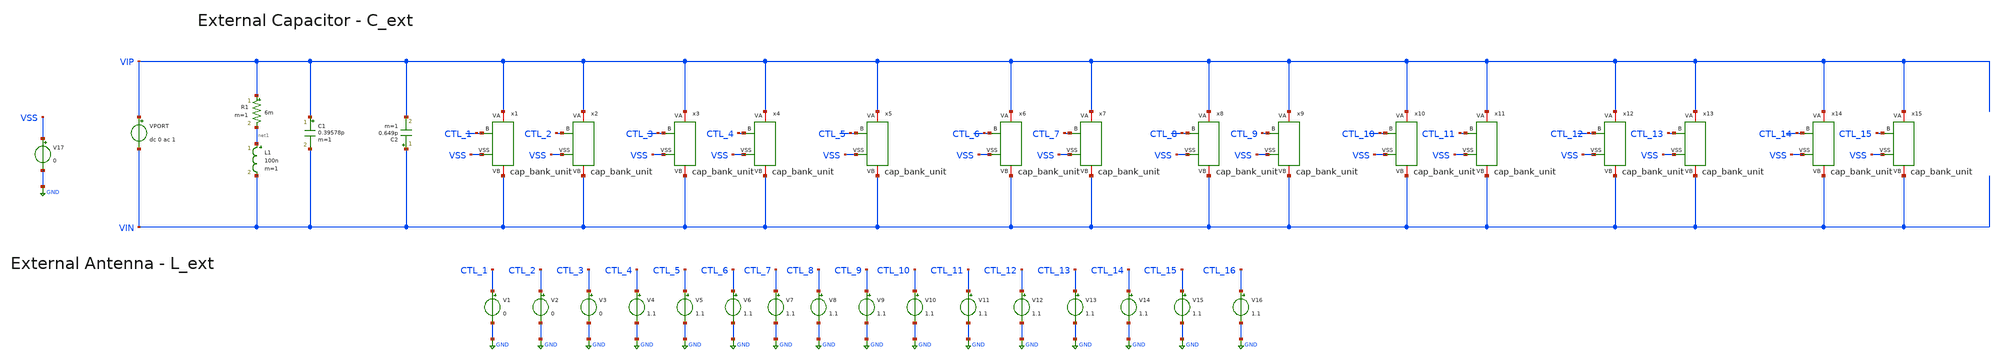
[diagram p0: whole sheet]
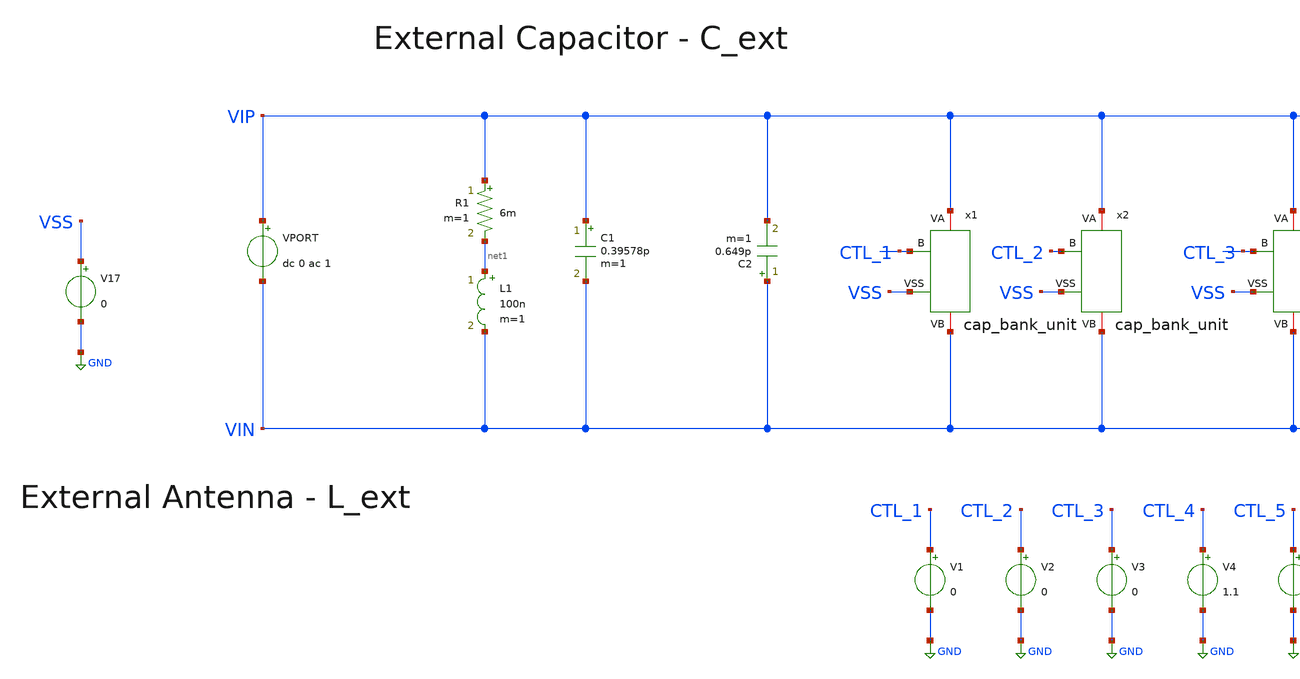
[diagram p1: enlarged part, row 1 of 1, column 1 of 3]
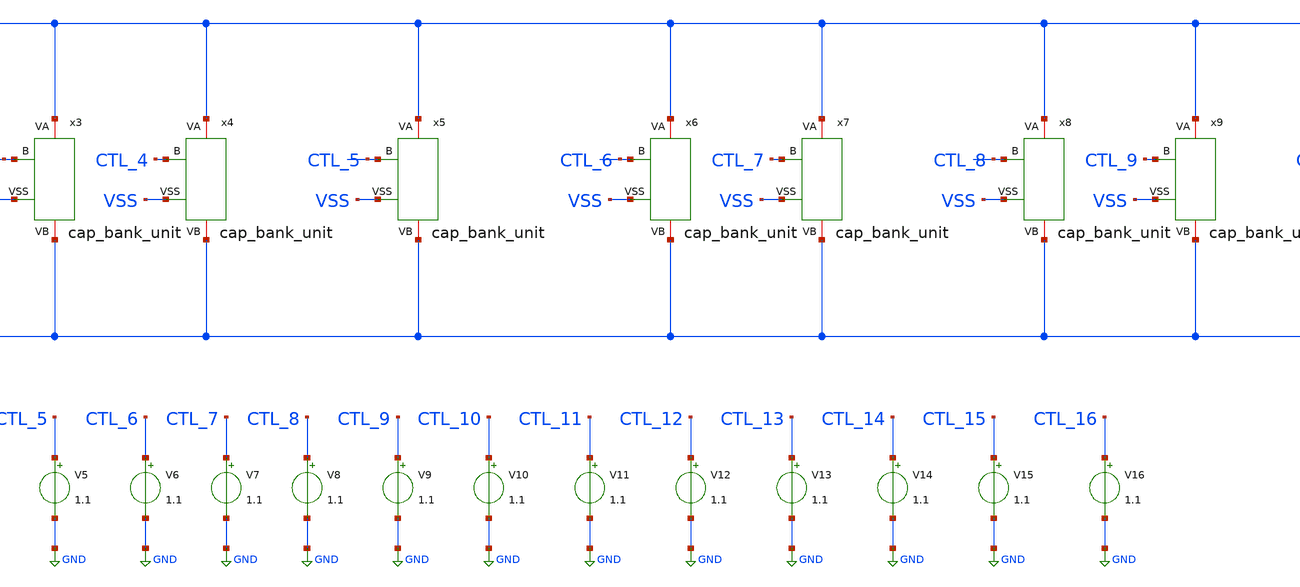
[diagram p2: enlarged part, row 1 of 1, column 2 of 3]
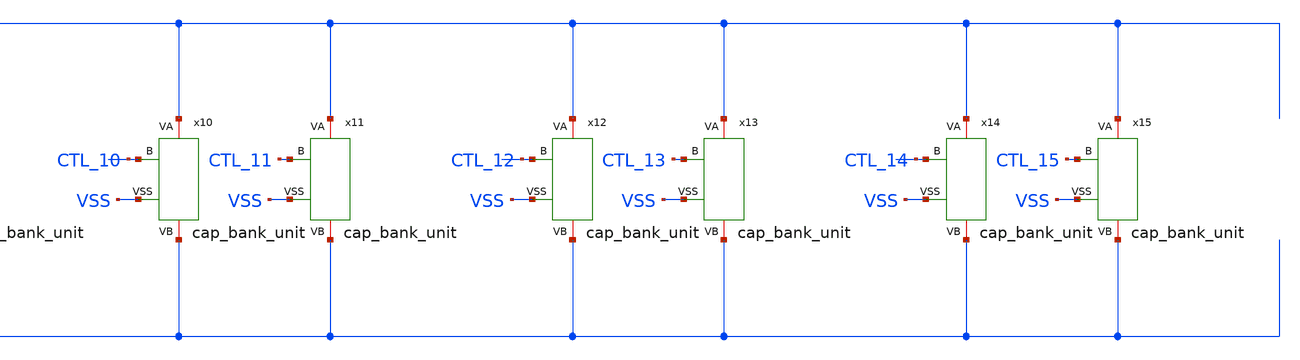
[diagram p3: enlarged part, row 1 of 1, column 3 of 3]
** sch_path: analog/tb/tb_cap_bank.sch
**.subckt tb_cap_bank
L1 net1 VIN 100n m=1
R1 VIP net1 6m m=1
C1 VIP VIN 0.39578p m=1
C2 VIN VIP 0.649p m=1
VPORT VIP VIN dc 0 ac 1
V1 CTL_1 GND 0
V2 CTL_2 GND 0
V3 CTL_3 GND 0
V4 CTL_4 GND 1.1
V5 CTL_5 GND 1.1
V6 CTL_6 GND 1.1
V7 CTL_7 GND 1.1
V8 CTL_8 GND 1.1
V9 CTL_9 GND 1.1
V10 CTL_10 GND 1.1
V11 CTL_11 GND 1.1
V12 CTL_12 GND 1.1
V13 CTL_13 GND 1.1
V14 CTL_14 GND 1.1
V15 CTL_15 GND 1.1
V16 CTL_16 GND 1.1
x1 VIP VSS CTL_1 VIN cap_bank_unit
V17 VSS GND 0
x2 VIP VSS CTL_2 VIN cap_bank_unit
x3 VIP VSS CTL_3 VIN cap_bank_unit
x4 VIP VSS CTL_4 VIN cap_bank_unit
x5 VIP VSS CTL_5 VIN cap_bank_unit
x6 VIP VSS CTL_6 VIN cap_bank_unit
x7 VIP VSS CTL_7 VIN cap_bank_unit
x8 VIP VSS CTL_8 VIN cap_bank_unit
x9 VIP VSS CTL_9 VIN cap_bank_unit
x10 VIP VSS CTL_10 VIN cap_bank_unit
x11 VIP VSS CTL_11 VIN cap_bank_unit
x12 VIP VSS CTL_12 VIN cap_bank_unit
x13 VIP VSS CTL_13 VIN cap_bank_unit
x14 VIP VSS CTL_14 VIN cap_bank_unit
x15 VIP VSS CTL_15 VIN cap_bank_unit
**** begin user architecture code



.save all
.save V(VIP) V(VIN) V(VIP, VIN)
.save I(VPORT)


.control
  set filetype=ascii        ; ASCII .raw (human-readable)

  foreach test_case 0 1 2 3 4 5 6 7 8 9 10 11 12 13 14 15
    if ($test_case = 0)
      alter v1 dc = 0
      alter v2 dc = 0
      alter v3 dc = 0
      alter v4 dc = 0
      alter v5 dc = 0
      alter v6 dc = 0
      alter v7 dc = 0
      alter v8 dc = 0
      alter v9 dc = 0
      alter v10 dc = 0
      alter v11 dc = 0
      alter v12 dc = 0
      alter v13 dc = 0
      alter v14 dc = 0
      alter v15 dc = 0
      alter v16 dc = 0
    else
      if ($test_case = 1)
      alter v1 dc = 1.2
      alter v2 dc = 0
      alter v3 dc = 0
      alter v4 dc = 0
      alter v5 dc = 0
      alter v6 dc = 0
      alter v7 dc = 0
      alter v8 dc = 0
      alter v9 dc = 0
      alter v10 dc = 0
      alter v11 dc = 0
      alter v12 dc = 0
      alter v13 dc = 0
      alter v14 dc = 0
      alter v15 dc = 0
      alter v16 dc = 0
      else
      if ($test_case = 2)
      alter v1 dc = 1.2
      alter v2 dc = 1.2
      alter v3 dc = 0
      alter v4 dc = 0
      alter v5 dc = 0
      alter v6 dc = 0
      alter v7 dc = 0
      alter v8 dc = 0
      alter v9 dc = 0
      alter v10 dc = 0
      alter v11 dc = 0
      alter v12 dc = 0
      alter v13 dc = 0
      alter v14 dc = 0
      alter v15 dc = 0
      alter v16 dc = 0
      else
      if ($test_case = 3)
      alter v1 dc = 1.2
      alter v2 dc = 1.2
      alter v3 dc = 1.2
      alter v4 dc = 0
      alter v5 dc = 0
      alter v6 dc = 0
      alter v7 dc = 0
      alter v8 dc = 0
      alter v9 dc = 0
      alter v10 dc = 0
      alter v11 dc = 0
      alter v12 dc = 0
      alter v13 dc = 0
      alter v14 dc = 0
      alter v15 dc = 0
      alter v16 dc = 0
      else
      if ($test_case = 4)
      alter v1 dc = 1.2
      alter v2 dc = 1.2
      alter v3 dc = 1.2
      alter v4 dc = 1.2
      alter v5 dc = 0
      alter v6 dc = 0
      alter v7 dc = 0
      alter v8 dc = 0
      alter v9 dc = 0
      alter v10 dc = 0
      alter v11 dc = 0
      alter v12 dc = 0
      alter v13 dc = 0
      alter v14 dc = 0
      alter v15 dc = 0
      alter v16 dc = 0
      else
      if ($test_case = 5)
      alter v1 dc = 1.2
      alter v2 dc = 1.2
      alter v3 dc = 1.2
      alter v4 dc = 1.2
      alter v5 dc = 1.2
      alter v6 dc = 0
      alter v7 dc = 0
      alter v8 dc = 0
      alter v9 dc = 0
      alter v10 dc = 0
      alter v11 dc = 0
      alter v12 dc = 0
      alter v13 dc = 0
      alter v14 dc = 0
      alter v15 dc = 0
      alter v16 dc = 0
      else
      if ($test_case = 6)
      alter v1 dc = 1.2
      alter v2 dc = 1.2
      alter v3 dc = 1.2
      alter v4 dc = 1.2
      alter v5 dc = 1.2
      alter v6 dc = 1.2
      alter v7 dc = 0
      alter v8 dc = 0
      alter v9 dc = 0
      alter v10 dc = 0
      alter v11 dc = 0
      alter v12 dc = 0
      alter v13 dc = 0
      alter v14 dc = 0
      alter v15 dc = 0
      alter v16 dc = 0
      else
      if ($test_case = 7)
      alter v1 dc = 1.2
      alter v2 dc = 1.2
      alter v3 dc = 1.2
      alter v4 dc = 1.2
      alter v5 dc = 1.2
      alter v6 dc = 1.2
      alter v7 dc = 1.2
      alter v8 dc = 0
      alter v9 dc = 0
      alter v10 dc = 0
      alter v11 dc = 0
      alter v12 dc = 0
      alter v13 dc = 0
      alter v14 dc = 0
      alter v15 dc = 0
      alter v16 dc = 0
      else
      if ($test_case = 8)
      alter v1 dc = 1.2
      alter v2 dc = 1.2
      alter v3 dc = 1.2
      alter v4 dc = 1.2
      alter v5 dc = 1.2
      alter v6 dc = 1.2
      alter v7 dc = 1.2
      alter v8 dc = 1.2
      alter v9 dc = 0
      alter v10 dc = 0
      alter v11 dc = 0
      alter v12 dc = 0
      alter v13 dc = 0
      alter v14 dc = 0
      alter v15 dc = 0
      alter v16 dc = 0
      else
      if ($test_case = 9)
      alter v1 dc = 1.2
      alter v2 dc = 1.2
      alter v3 dc = 1.2
      alter v4 dc = 1.2
      alter v5 dc = 1.2
      alter v6 dc = 1.2
      alter v7 dc = 1.2
      alter v8 dc = 1.2
      alter v9 dc = 1.2
      alter v10 dc = 0
      alter v11 dc = 0
      alter v12 dc = 0
      alter v13 dc = 0
      alter v14 dc = 0
      alter v15 dc = 0
      alter v16 dc = 0
      else
      if ($test_case = 10)
      alter v1 dc = 1.2
      alter v2 dc = 1.2
      alter v3 dc = 1.2
      alter v4 dc = 1.2
      alter v5 dc = 1.2
      alter v6 dc = 1.2
      alter v7 dc = 1.2
      alter v8 dc = 1.2
      alter v9 dc = 1.2
      alter v10 dc = 1.2
      alter v11 dc = 0
      alter v12 dc = 0
      alter v13 dc = 0
      alter v14 dc = 0
      alter v15 dc = 0
      alter v16 dc = 0
      else
      if ($test_case = 11)
      alter v1 dc = 1.2
      alter v2 dc = 1.2
      alter v3 dc = 1.2
      alter v4 dc = 1.2
      alter v5 dc = 1.2
      alter v6 dc = 1.2
      alter v7 dc = 1.2
      alter v8 dc = 1.2
      alter v9 dc = 1.2
      alter v10 dc = 1.2
      alter v11 dc = 1.2
      alter v12 dc = 0
      alter v13 dc = 0
      alter v14 dc = 0
      alter v15 dc = 0
      alter v16 dc = 0
      else
      if ($test_case = 12)
      alter v1 dc = 1.2
      alter v2 dc = 1.2
      alter v3 dc = 1.2
      alter v4 dc = 1.2
      alter v5 dc = 1.2
      alter v6 dc = 1.2
      alter v7 dc = 1.2
      alter v8 dc = 1.2
      alter v9 dc = 1.2
      alter v10 dc = 1.2
      alter v11 dc = 1.2
      alter v12 dc = 1.2
      alter v13 dc = 0
      alter v14 dc = 0
      alter v15 dc = 0
      alter v16 dc = 0
      else
      if ($test_case = 13)
      alter v1 dc = 1.2
      alter v2 dc = 1.2
      alter v3 dc = 1.2
      alter v4 dc = 1.2
      alter v5 dc = 1.2
      alter v6 dc = 1.2
      alter v7 dc = 1.2
      alter v8 dc = 1.2
      alter v9 dc = 1.2
      alter v10 dc = 1.2
      alter v11 dc = 1.2
      alter v12 dc = 1.2
      alter v13 dc = 1.2
      alter v14 dc = 0
      alter v15 dc = 0
      alter v16 dc = 0
      else
      if ($test_case = 14)
      alter v1 dc = 1.2
      alter v2 dc = 1.2
      alter v3 dc = 1.2
      alter v4 dc = 1.2
      alter v5 dc = 1.2
      alter v6 dc = 1.2
      alter v7 dc = 1.2
      alter v8 dc = 1.2
      alter v9 dc = 1.2
      alter v10 dc = 1.2
      alter v11 dc = 1.2
      alter v12 dc = 1.2
      alter v13 dc = 1.2
      alter v14 dc = 1.2
      alter v15 dc = 0
      alter v16 dc = 0
      else
      if ($test_case = 15)
      alter v1 dc = 1.2
      alter v2 dc = 1.2
      alter v3 dc = 1.2
      alter v4 dc = 1.2
      alter v5 dc = 1.2
      alter v6 dc = 1.2
      alter v7 dc = 1.2
      alter v8 dc = 1.2
      alter v9 dc = 1.2
      alter v10 dc = 1.2
      alter v11 dc = 1.2
      alter v12 dc = 1.2
      alter v13 dc = 1.2
      alter v14 dc = 1.2
      alter v15 dc = 1.2
      alter v16 dc = 0
      else
      alter v1 dc = 1.2
      alter v2 dc = 1.2
      alter v3 dc = 1.2
      alter v4 dc = 1.2
      alter v5 dc = 1.2
      alter v6 dc = 1.2
      alter v7 dc = 1.2
      alter v8 dc = 1.2
      alter v9 dc = 1.2
      alter v10 dc = 1.2
      alter v11 dc = 1.2
      alter v12 dc = 1.2
      alter v13 dc = 1.2
      alter v14 dc = 1.2
      alter v15 dc = 1.2
      alter v16 dc = 1.2
      end
      end
      end
      end
      end
      end
      end
      end
      end
      end
      end
      end
      end
      end
      end
    end

    run
    ac lin 5000 300Meg 600Meg
    *tran 0.1u 100u
    let ZIN  = v(VIP, VIN)/i(VPORT)
    let ABSZ = abs(ZIN)
    let IMZ  = imag(ZIN)
    let REZ  = real(ZIN)
    meas ac F_res when IMZ=0
    write tb_capb.raw ABSZ
    set appendwrite
  end
.endc



.lib cornerMOSlv.lib mos_tt

**** end user architecture code
**.ends

* expanding   symbol:  cap_bank_unit.sym # of pins=4
** sym_path: analog/core/cap_bank_unit.sym
** sch_path: analog/core/cap_bank_unit.sch
.subckt cap_bank_unit VA VSS B VB
*.iopin VA
*.iopin VSS
*.iopin B
*.iopin VB
C1 VA net2 68.84f m=1
C2 VB net1 68.84f m=1
XM1 net2 B net1 VSS sg13_lv_nmos w=6.23u l=0.13u ng=1 m=1 mm_ok=1
XM2 net1 B VSS VSS sg13_lv_nmos w=6.23u l=0.13u ng=1 m=1 mm_ok=1
XM3 net2 B VSS VSS sg13_lv_nmos w=6.23u l=0.13u ng=1 m=1 mm_ok=1
.ends

.GLOBAL GND
.end
